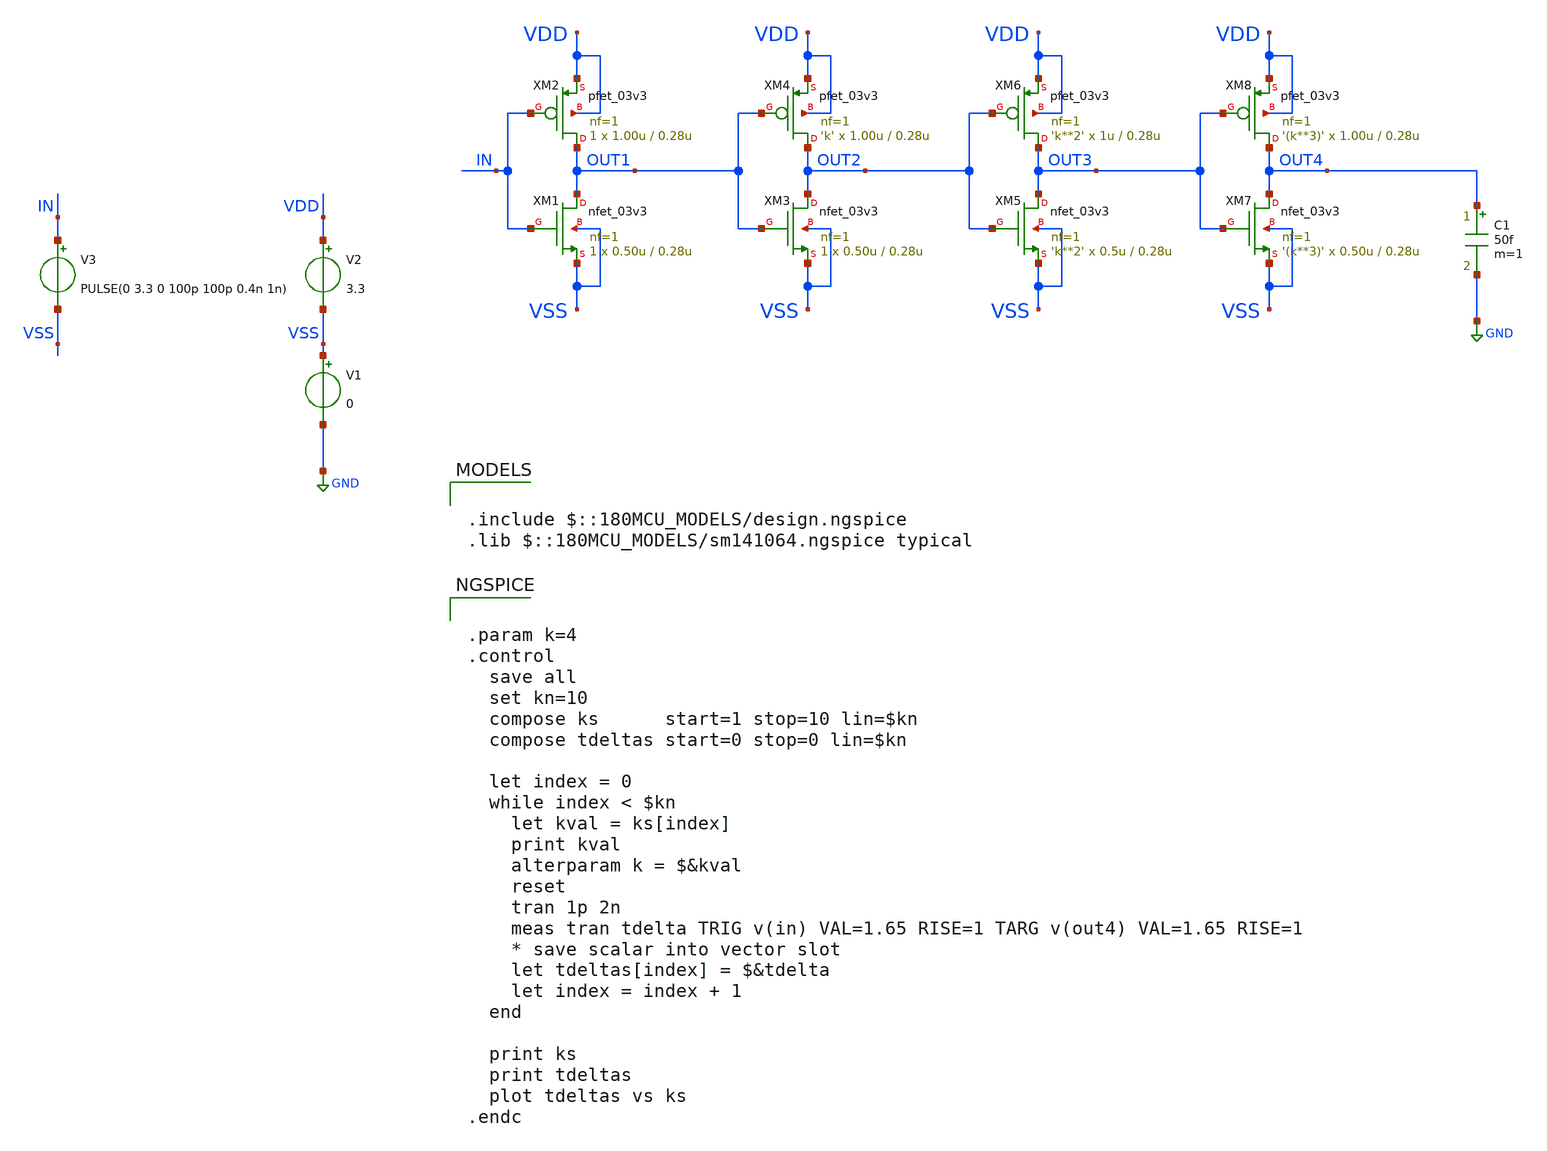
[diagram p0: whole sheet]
** sch_path: CAD6/DFF_Ray/example_inv_chain_sweep.sch
**.subckt example_inv_chain_sweep
XM1 OUT1 IN VSS VSS nfet_03v3 L=0.28u W=0.50u nf=1 ad='int((nf+1)/2) * W/nf * 0.18u' as='int((nf+2)/2) * W/nf * 0.18u'
+ pd='2*int((nf+1)/2) * (W/nf + 0.18u)' ps='2*int((nf+2)/2) * (W/nf + 0.18u)' nrd='0.18u / W' nrs='0.18u / W'
+ sa=0 sb=0 sd=0 m=1
XM2 OUT1 IN VDD VDD pfet_03v3 L=0.28u W=1.00u nf=1 ad='int((nf+1)/2) * W/nf * 0.18u' as='int((nf+2)/2) * W/nf * 0.18u'
+ pd='2*int((nf+1)/2) * (W/nf + 0.18u)' ps='2*int((nf+2)/2) * (W/nf + 0.18u)' nrd='0.18u / W' nrs='0.18u / W'
+ sa=0 sb=0 sd=0 m=1
XM3 OUT2 OUT1 VSS VSS nfet_03v3 L=0.28u W=0.50u nf=1 ad='int((nf+1)/2) * W/nf * 0.18u' as='int((nf+2)/2) * W/nf * 0.18u'
+ pd='2*int((nf+1)/2) * (W/nf + 0.18u)' ps='2*int((nf+2)/2) * (W/nf + 0.18u)' nrd='0.18u / W' nrs='0.18u / W'
+ sa=0 sb=0 sd=0 m=1
XM4 OUT2 OUT1 VDD VDD pfet_03v3 L=0.28u W=1.00u nf=1 ad='int((nf+1)/2) * W/nf * 0.18u' as='int((nf+2)/2) * W/nf * 0.18u'
+ pd='2*int((nf+1)/2) * (W/nf + 0.18u)' ps='2*int((nf+2)/2) * (W/nf + 0.18u)' nrd='0.18u / W' nrs='0.18u / W'
+ sa=0 sb=0 sd=0 m='k'
XM5 OUT3 OUT2 VSS VSS nfet_03v3 L=0.28u W=0.5u nf=1 ad='int((nf+1)/2) * W/nf * 0.18u' as='int((nf+2)/2) * W/nf * 0.18u'
+ pd='2*int((nf+1)/2) * (W/nf + 0.18u)' ps='2*int((nf+2)/2) * (W/nf + 0.18u)' nrd='0.18u / W' nrs='0.18u / W'
+ sa=0 sb=0 sd=0 m='k**2'
XM6 OUT3 OUT2 VDD VDD pfet_03v3 L=0.28u W=1u nf=1 ad='int((nf+1)/2) * W/nf * 0.18u' as='int((nf+2)/2) * W/nf * 0.18u'
+ pd='2*int((nf+1)/2) * (W/nf + 0.18u)' ps='2*int((nf+2)/2) * (W/nf + 0.18u)' nrd='0.18u / W' nrs='0.18u / W'
+ sa=0 sb=0 sd=0 m='k**2'
V1 VSS GND 0
V2 VDD VSS 3.3
V3 IN VSS PULSE(0 3.3 0 100p 100p 0.4n 1n)
C1 OUT4 GND 50f m=1
XM7 OUT4 OUT3 VSS VSS nfet_03v3 L=0.28u W=0.50u nf=1 ad='int((nf+1)/2) * W/nf * 0.18u' as='int((nf+2)/2) * W/nf * 0.18u'
+ pd='2*int((nf+1)/2) * (W/nf + 0.18u)' ps='2*int((nf+2)/2) * (W/nf + 0.18u)' nrd='0.18u / W' nrs='0.18u / W'
+ sa=0 sb=0 sd=0 m='(k**3)'
XM8 OUT4 OUT3 VDD VDD pfet_03v3 L=0.28u W=1.00u nf=1 ad='int((nf+1)/2) * W/nf * 0.18u' as='int((nf+2)/2) * W/nf * 0.18u'
+ pd='2*int((nf+1)/2) * (W/nf + 0.18u)' ps='2*int((nf+2)/2) * (W/nf + 0.18u)' nrd='0.18u / W' nrs='0.18u / W'
+ sa=0 sb=0 sd=0 m='(k**3)'
**** begin user architecture code

.include $::180MCU_MODELS/design.ngspice
.lib $::180MCU_MODELS/sm141064.ngspice typical



.param k=4
.control
  save all
  set kn=10
  compose ks      start=1 stop=10 lin=$kn
  compose tdeltas start=0 stop=0 lin=$kn

  let index = 0
  while index < $kn
    let kval = ks[index]
    print kval
    alterparam k = $&kval
    reset
    tran 1p 2n
    meas tran tdelta TRIG v(in) VAL=1.65 RISE=1 TARG v(out4) VAL=1.65 RISE=1
    * save scalar into vector slot
    let tdeltas[index] = $&tdelta
    let index = index + 1
  end

  print ks
  print tdeltas
  plot tdeltas vs ks
.endc


**** end user architecture code
**.ends
.GLOBAL GND
.end
